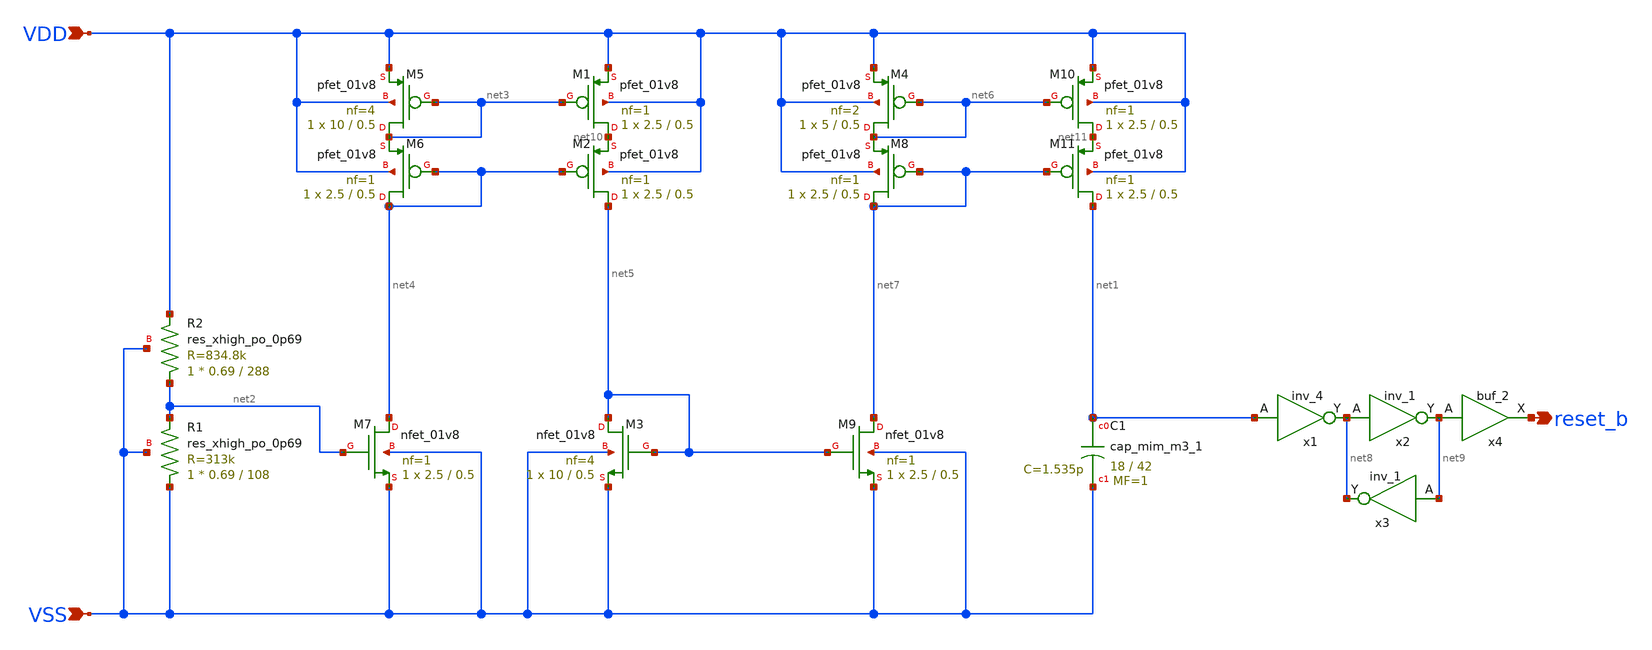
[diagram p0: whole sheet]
** sch_path: xschem/por.sch
**.subckt por VDD VSS reset_b
*.ipin VDD
*.ipin VSS
*.opin reset_b
XC1 net1 VSS sky130_fd_pr__cap_mim_m3_1 W=18 L=42 MF=1 m=1
x1 net1 VSS VSS VDD VDD net8 sky130_fd_sc_hd__inv_4
XR1 VSS net2 VSS sky130_fd_pr__res_xhigh_po_0p69 L=108 mult=1 m=1
XM5 net3 net3 VDD VDD sky130_fd_pr__pfet_01v8 L=0.5 W=10 nf=4 ad='int((nf+1)/2) * W/nf * 0.29' as='int((nf+2)/2) * W/nf * 0.29'
+ pd='2*int((nf+1)/2) * (W/nf + 0.29)' ps='2*int((nf+2)/2) * (W/nf + 0.29)' nrd='0.29 / W' nrs='0.29 / W'
+ sa=0 sb=0 sd=0 mult=1 m=1
XM6 net4 net4 net3 VDD sky130_fd_pr__pfet_01v8 L=0.5 W=2.5 nf=1 ad='int((nf+1)/2) * W/nf * 0.29' as='int((nf+2)/2) * W/nf * 0.29'
+ pd='2*int((nf+1)/2) * (W/nf + 0.29)' ps='2*int((nf+2)/2) * (W/nf + 0.29)' nrd='0.29 / W' nrs='0.29 / W'
+ sa=0 sb=0 sd=0 mult=1 m=1
XM7 net4 net2 VSS VSS sky130_fd_pr__nfet_01v8 L=0.5 W=2.5 nf=1 ad='int((nf+1)/2) * W/nf * 0.29' as='int((nf+2)/2) * W/nf * 0.29'
+ pd='2*int((nf+1)/2) * (W/nf + 0.29)' ps='2*int((nf+2)/2) * (W/nf + 0.29)' nrd='0.29 / W' nrs='0.29 / W'
+ sa=0 sb=0 sd=0 mult=1 m=1
XR2 net2 VDD VSS sky130_fd_pr__res_xhigh_po_0p69 L=288 mult=1 m=1
XM1 net10 net3 VDD VDD sky130_fd_pr__pfet_01v8 L=0.5 W=2.5 nf=1 ad='int((nf+1)/2) * W/nf * 0.29' as='int((nf+2)/2) * W/nf * 0.29'
+ pd='2*int((nf+1)/2) * (W/nf + 0.29)' ps='2*int((nf+2)/2) * (W/nf + 0.29)' nrd='0.29 / W' nrs='0.29 / W'
+ sa=0 sb=0 sd=0 mult=1 m=1
XM2 net5 net4 net10 VDD sky130_fd_pr__pfet_01v8 L=0.5 W=2.5 nf=1 ad='int((nf+1)/2) * W/nf * 0.29' as='int((nf+2)/2) * W/nf * 0.29'
+ pd='2*int((nf+1)/2) * (W/nf + 0.29)' ps='2*int((nf+2)/2) * (W/nf + 0.29)' nrd='0.29 / W' nrs='0.29 / W'
+ sa=0 sb=0 sd=0 mult=1 m=1
XM3 net5 net5 VSS VSS sky130_fd_pr__nfet_01v8 L=0.5 W=10 nf=4 ad='int((nf+1)/2) * W/nf * 0.29' as='int((nf+2)/2) * W/nf * 0.29'
+ pd='2*int((nf+1)/2) * (W/nf + 0.29)' ps='2*int((nf+2)/2) * (W/nf + 0.29)' nrd='0.29 / W' nrs='0.29 / W'
+ sa=0 sb=0 sd=0 mult=1 m=1
XM4 net6 net6 VDD VDD sky130_fd_pr__pfet_01v8 L=0.5 W=5 nf=2 ad='int((nf+1)/2) * W/nf * 0.29' as='int((nf+2)/2) * W/nf * 0.29'
+ pd='2*int((nf+1)/2) * (W/nf + 0.29)' ps='2*int((nf+2)/2) * (W/nf + 0.29)' nrd='0.29 / W' nrs='0.29 / W'
+ sa=0 sb=0 sd=0 mult=1 m=1
XM8 net7 net7 net6 VDD sky130_fd_pr__pfet_01v8 L=0.5 W=2.5 nf=1 ad='int((nf+1)/2) * W/nf * 0.29' as='int((nf+2)/2) * W/nf * 0.29'
+ pd='2*int((nf+1)/2) * (W/nf + 0.29)' ps='2*int((nf+2)/2) * (W/nf + 0.29)' nrd='0.29 / W' nrs='0.29 / W'
+ sa=0 sb=0 sd=0 mult=1 m=1
XM9 net7 net5 VSS VSS sky130_fd_pr__nfet_01v8 L=0.5 W=2.5 nf=1 ad='int((nf+1)/2) * W/nf * 0.29' as='int((nf+2)/2) * W/nf * 0.29'
+ pd='2*int((nf+1)/2) * (W/nf + 0.29)' ps='2*int((nf+2)/2) * (W/nf + 0.29)' nrd='0.29 / W' nrs='0.29 / W'
+ sa=0 sb=0 sd=0 mult=1 m=1
XM10 net11 net6 VDD VDD sky130_fd_pr__pfet_01v8 L=0.5 W=2.5 nf=1 ad='int((nf+1)/2) * W/nf * 0.29' as='int((nf+2)/2) * W/nf * 0.29'
+ pd='2*int((nf+1)/2) * (W/nf + 0.29)' ps='2*int((nf+2)/2) * (W/nf + 0.29)' nrd='0.29 / W' nrs='0.29 / W'
+ sa=0 sb=0 sd=0 mult=1 m=1
XM11 net1 net7 net11 VDD sky130_fd_pr__pfet_01v8 L=0.5 W=2.5 nf=1 ad='int((nf+1)/2) * W/nf * 0.29' as='int((nf+2)/2) * W/nf * 0.29'
+ pd='2*int((nf+1)/2) * (W/nf + 0.29)' ps='2*int((nf+2)/2) * (W/nf + 0.29)' nrd='0.29 / W' nrs='0.29 / W'
+ sa=0 sb=0 sd=0 mult=1 m=1
x2 net8 VSS VSS VDD VDD net9 sky130_fd_sc_hd__inv_1
x3 net9 VSS VSS VDD VDD net8 sky130_fd_sc_hd__inv_1
x4 net9 VSS VSS VDD VDD reset_b sky130_fd_sc_hd__buf_2
**.ends
.end
